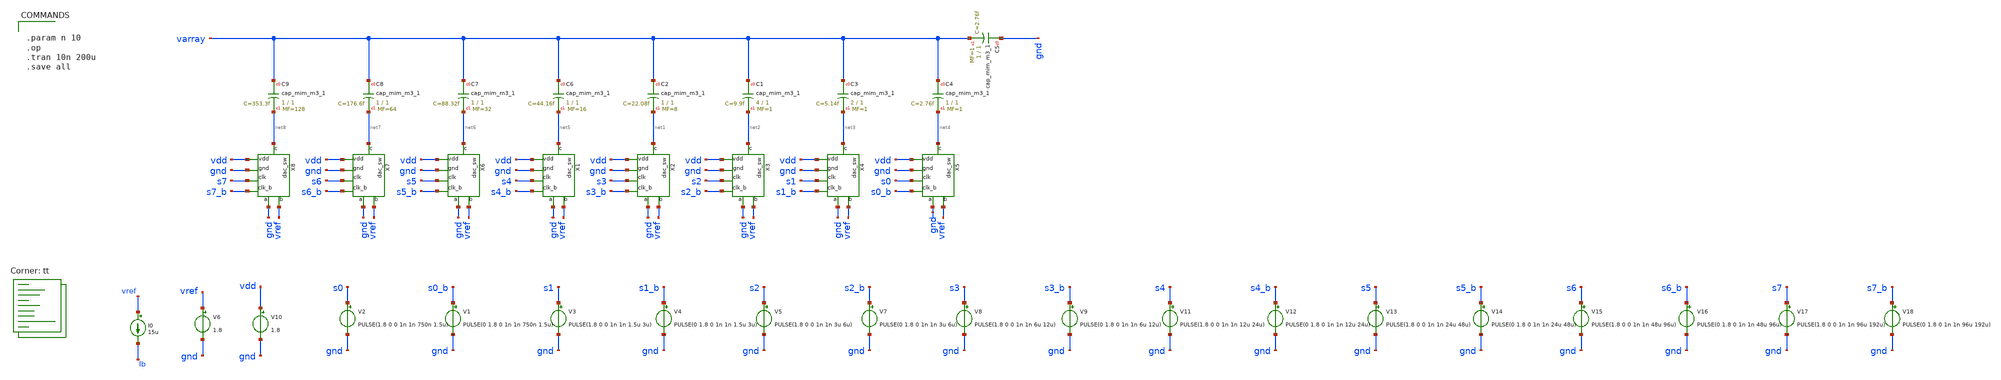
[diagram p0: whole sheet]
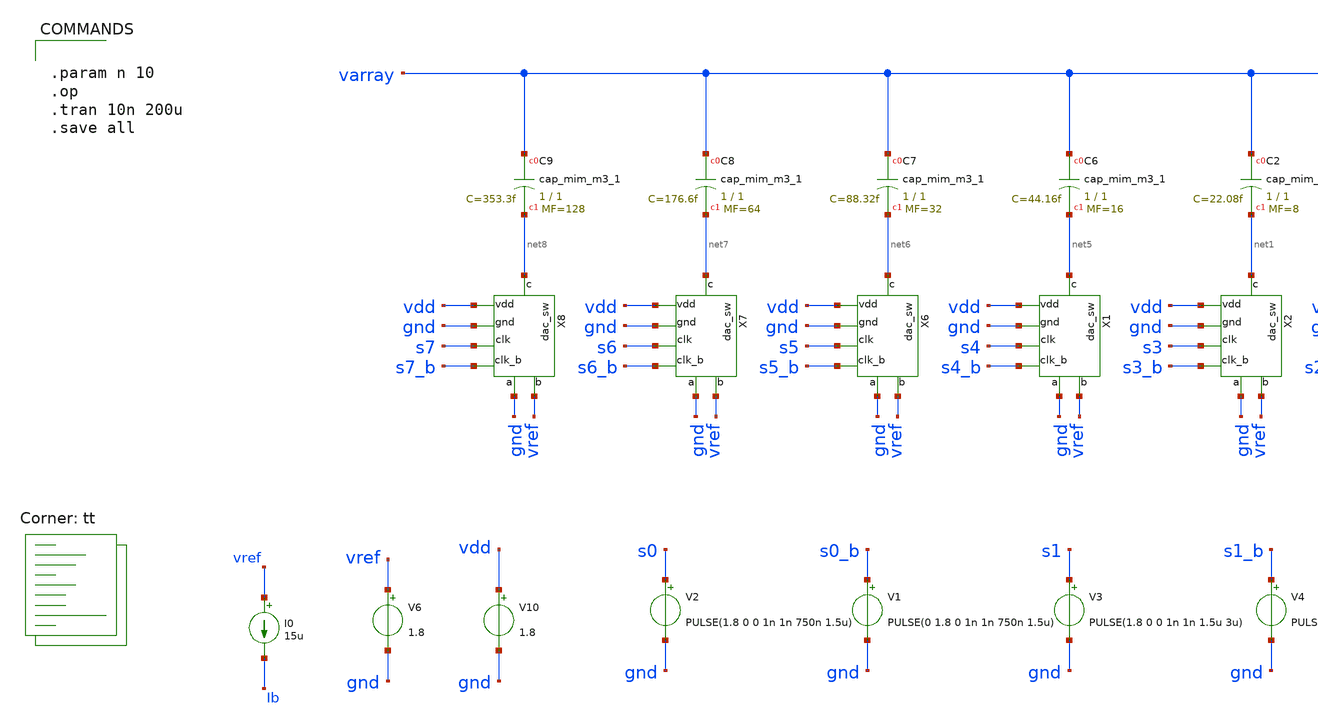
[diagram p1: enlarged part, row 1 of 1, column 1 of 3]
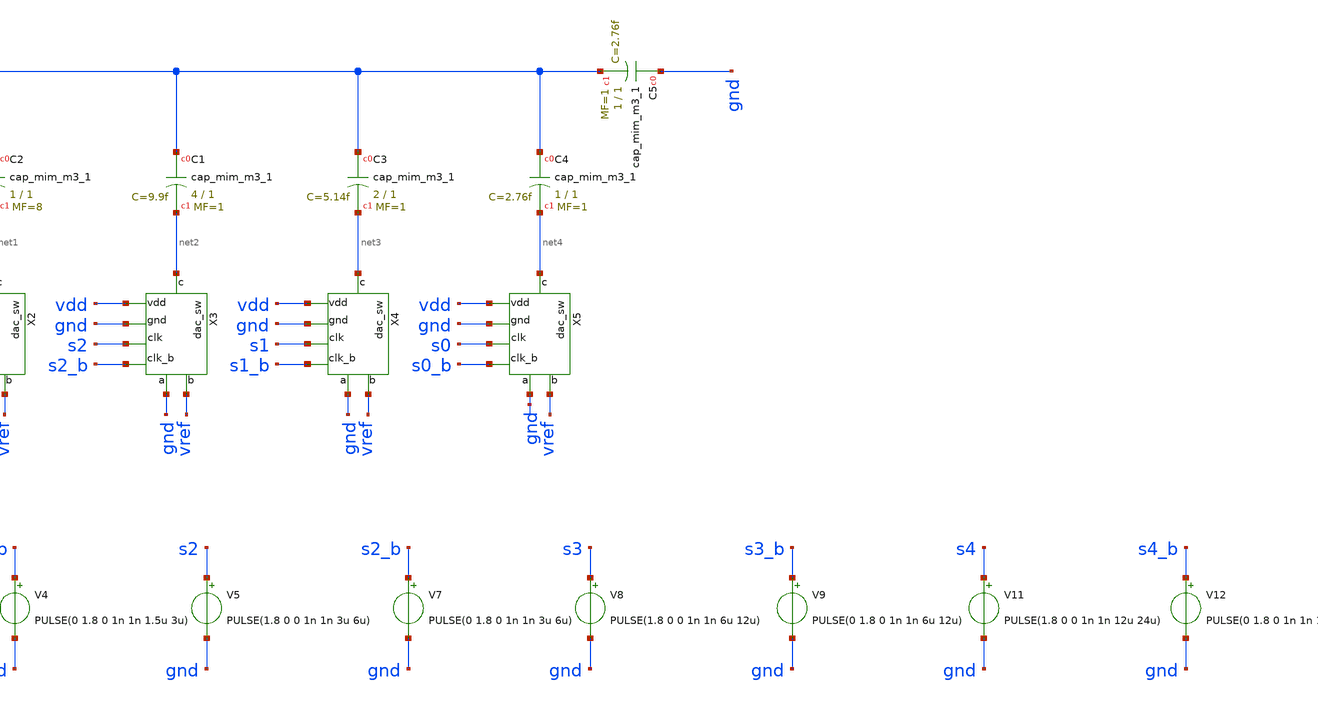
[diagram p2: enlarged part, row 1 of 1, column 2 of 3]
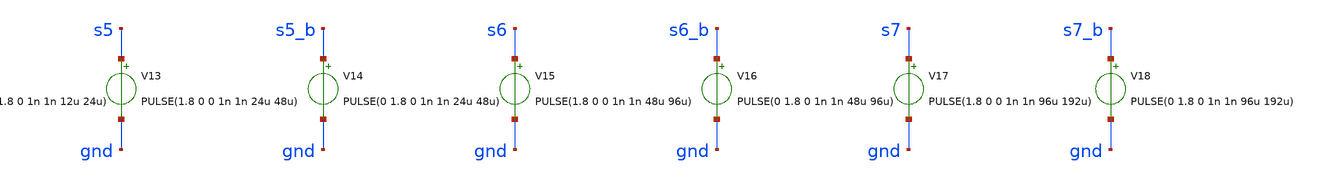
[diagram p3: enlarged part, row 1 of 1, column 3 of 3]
** sch_path: xschem/dac/dac.sch
**.subckt dac
XC2 varray net1 sky130_fd_pr__cap_mim_m3_1 W=1 L=1 MF=8 m=8
V2 s0 gnd PULSE(1.8 0 0 1n 1n 750n 1.5u)
V6 vref gnd 1.8
V1 s0_b gnd PULSE(0 1.8 0 1n 1n 750n 1.5u)
V3 s1 gnd PULSE(1.8 0 0 1n 1n 1.5u 3u)
V4 s1_b gnd PULSE(0 1.8 0 1n 1n 1.5u 3u)
V5 s2 gnd PULSE(1.8 0 0 1n 1n 3u 6u)
V7 s2_b gnd PULSE(0 1.8 0 1n 1n 3u 6u)
V8 s3 gnd PULSE(1.8 0 0 1n 1n 6u 12u)
V9 s3_b gnd PULSE(0 1.8 0 1n 1n 6u 12u)
I0 vref Ib 15u
V10 vdd gnd 1.8
X2 net1 vref gnd vdd s3 s3_b gnd dac_sw
XC1 varray net2 sky130_fd_pr__cap_mim_m3_1 W=4 L=1 MF=1 m=1
X3 net2 vref gnd vdd s2 s2_b gnd dac_sw
X4 net3 vref gnd vdd s1 s1_b gnd dac_sw
X5 net4 vref gnd vdd s0 s0_b gnd dac_sw
XC3 varray net3 sky130_fd_pr__cap_mim_m3_1 W=2 L=1 MF=1 m=1
XC4 varray net4 sky130_fd_pr__cap_mim_m3_1 W=1 L=1 MF=1 m=1
XC5 gnd varray sky130_fd_pr__cap_mim_m3_1 W=1 L=1 MF=1 m=1
XC6 varray net5 sky130_fd_pr__cap_mim_m3_1 W=1 L=1 MF=16 m=16
X1 net5 vref gnd vdd s4 s4_b gnd dac_sw
XC7 varray net6 sky130_fd_pr__cap_mim_m3_1 W=1 L=1 MF=32 m=32
X6 net6 vref gnd vdd s5 s5_b gnd dac_sw
XC8 varray net7 sky130_fd_pr__cap_mim_m3_1 W=1 L=1 MF=64 m=64
X7 net7 vref gnd vdd s6 s6_b gnd dac_sw
XC9 varray net8 sky130_fd_pr__cap_mim_m3_1 W=1 L=1 MF=128 m=128
X8 net8 vref gnd vdd s7 s7_b gnd dac_sw
V11 s4 gnd PULSE(1.8 0 0 1n 1n 12u 24u)
V12 s4_b gnd PULSE(0 1.8 0 1n 1n 12u 24u)
V13 s5 gnd PULSE(1.8 0 0 1n 1n 24u 48u)
V14 s5_b gnd PULSE(0 1.8 0 1n 1n 24u 48u)
V15 s6 gnd PULSE(1.8 0 0 1n 1n 48u 96u)
V16 s6_b gnd PULSE(0 1.8 0 1n 1n 48u 96u)
V17 s7 gnd PULSE(1.8 0 0 1n 1n 96u 192u)
V18 s7_b gnd PULSE(0 1.8 0 1n 1n 96u 192u)
**** begin user architecture code
.lib $::SKYWATER_MODELS/sky130.lib.spice tt


.param n 10
.op
.tran 10n 200u
.save all


**** end user architecture code
**.ends

* expanding   symbol:  xschem/dac/dac_sw.sym # of pins=7
** sym_path: xschem/dac/dac_sw.sym
** sch_path: xschem/dac/dac_sw.sch
.subckt dac_sw c b gnd vdd clk clk_b a
*.iopin vdd
*.iopin gnd
*.ipin clk
*.ipin clk_b
*.iopin c
*.iopin a
*.iopin b
XM2 c clk b gnd sky130_fd_pr__nfet_01v8 L=0.15 W=10 nf=1 ad='int((nf+1)/2) * W/nf * 0.29' as='int((nf+2)/2) * W/nf * 0.29'
+ pd='2*int((nf+1)/2) * (W/nf + 0.29)' ps='2*int((nf+2)/2) * (W/nf + 0.29)' nrd='0.29 / W' nrs='0.29 / W'
+ sa=0 sb=0 sd=0 mult=1 m=1
XM5 b clk_b c vdd sky130_fd_pr__pfet_01v8 L=0.15 W=20 nf=1 ad='int((nf+1)/2) * W/nf * 0.29' as='int((nf+2)/2) * W/nf * 0.29'
+ pd='2*int((nf+1)/2) * (W/nf + 0.29)' ps='2*int((nf+2)/2) * (W/nf + 0.29)' nrd='0.29 / W' nrs='0.29 / W'
+ sa=0 sb=0 sd=0 mult=1 m=1
XM6 c clk_b a gnd sky130_fd_pr__nfet_01v8 L=0.15 W=10 nf=1 ad='int((nf+1)/2) * W/nf * 0.29' as='int((nf+2)/2) * W/nf * 0.29'
+ pd='2*int((nf+1)/2) * (W/nf + 0.29)' ps='2*int((nf+2)/2) * (W/nf + 0.29)' nrd='0.29 / W' nrs='0.29 / W'
+ sa=0 sb=0 sd=0 mult=1 m=1
XM7 a clk c vdd sky130_fd_pr__pfet_01v8 L=0.15 W=20 nf=1 ad='int((nf+1)/2) * W/nf * 0.29' as='int((nf+2)/2) * W/nf * 0.29'
+ pd='2*int((nf+1)/2) * (W/nf + 0.29)' ps='2*int((nf+2)/2) * (W/nf + 0.29)' nrd='0.29 / W' nrs='0.29 / W'
+ sa=0 sb=0 sd=0 mult=1 m=1
.ends

.end
